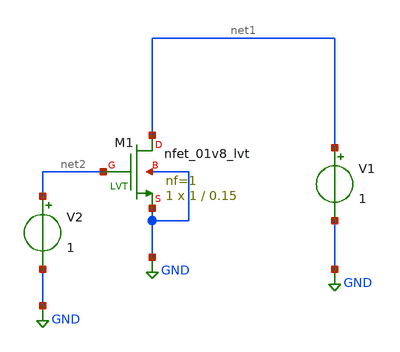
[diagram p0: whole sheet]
** sch_path: gmid_char/test.sch
**.subckt test
V1 net1 GND 1
V2 net2 GND 1
XM1 net1 net2 GND GND sky130_fd_pr__nfet_01v8_lvt L=0.15 W=1 nf=1 ad='int((nf+1)/2) * W/nf * 0.29' as='int((nf+2)/2) * W/nf * 0.29'
+ pd='2*int((nf+1)/2) * (W/nf + 0.29)' ps='2*int((nf+2)/2) * (W/nf + 0.29)' nrd='0.29 / W' nrs='0.29 / W'
+ sa=0 sb=0 sd=0 mult=1 m=1
**** begin user architecture code



.lib /usr/local/share/pdk/sky130A/libs.tech/ngspice/sky130.lib.spice tt
.option wnflag=1

.control
save all

save @m.xm1.msky130_fd_pr__nfet_01v8_lvt[gm]
save @m.xm1.msky130_fd_pr__nfet_01v8_lvt[id]
save @m.xm1.msky130_fd_pr__nfet_01v8_lvt[gds]
save @m.xm1.msky130_fd_pr__nfet_01v8_lvt[cgg]
save @m.xm1.msky130_fd_pr__nfet_01v8_lvt[vdsat]

dc v2 0 1 1m

let gm = @m.xm1.msky130_fd_pr__nfet_01v8_lvt[gm]
let id = @m.xm1.msky130_fd_pr__nfet_01v8_lvt[id]
let gds = @m.xm1.msky130_fd_pr__nfet_01v8_lvt[gds]
let cgg = @m.xm1.msky130_fd_pr__nfet_01v8_lvt[cgg]
let vdsat = @m.xm1.msky130_fd_pr__nfet_01v8_lvt[vdsat]

let gain = gm/gds
let ft = gm/(2*3.1415*cgg)
let gmoverid = gm/id

plot gain
plot ft
plot gmoverid
plot id
plot vdsat

wrdata gain.txt gain
wrdata ft.txt ft
wrdata gmoverid.txt gmoverid
wrdata id.txt id

.endc




**** end user architecture code
**.ends
.GLOBAL GND
.end
